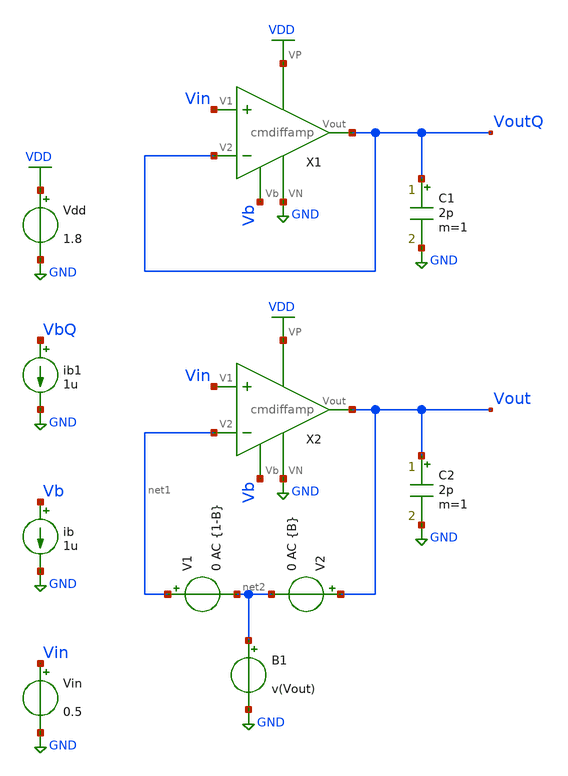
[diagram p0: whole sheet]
** sch_path: projects/current_mirror_diff_amp/xschem_ngspice/cmdiffamp_loopgain.sch
**.subckt cmdiffamp_loopgain
X1 Vin VoutQ VoutQ VDD GND Vb cmdiffamp
Vin Vin GND 0.5
Vdd VDD GND 1.8
ib Vb GND 1u
C1 VoutQ GND 2p m=1
ib1 VbQ GND 1u
X2 Vin net1 Vout VDD GND Vb cmdiffamp
C2 Vout GND 2p m=1
V1 net1 net2 0 AC {1-B}
V2 Vout net2 0 AC {B}
B1 net2 GND v(Vout)
**** begin user architecture code



.lib /foss/pdks/sky130A/libs.tech/ngspice/sky130.lib.spice tt

.param B=0
.control
ac dec 20 1 1e12
alterparam B=1
reset
ac dec 20 1 1e12
setplot new
set curplottitle=Loopgain
let frequency=ac1.frequency
let T = (ac1.i(V2) + ac2.i(V1)) / (ac1.i(V1) + ac2.i(V2))
let Tmag = db(T)
let Tphase = 180*cph(T)/pi
plot Tmag Tphase xlog
.endc



**** end user architecture code
**.ends

* expanding   symbol:
*+  /foss/designs/my_design/projects/current_mirror_diff_amp/xschem_ngspice/cmdiffamp.sym # of pins=6
** sym_path: projects/current_mirror_diff_amp/xschem_ngspice/cmdiffamp.sym
** sch_path: projects/current_mirror_diff_amp/xschem_ngspice/cmdiffamp.sch
.subckt cmdiffamp V1 V2 Vout VP VN Vb
*.ipin V1
*.ipin V2
*.opin Vout
*.iopin VN
*.iopin Vb
*.iopin VP
XM1a net3 V1 net1 VDD sky130_fd_pr__pfet_01v8 L=0.5 W=3 nf=1 ad='int((nf+1)/2) * W/nf * 0.29' as='int((nf+2)/2) * W/nf * 0.29'
+ pd='2*int((nf+1)/2) * (W/nf + 0.29)' ps='2*int((nf+2)/2) * (W/nf + 0.29)' nrd='0.29 / W' nrs='0.29 / W'
+ sa=0 sb=0 sd=0 mult=1 m=1
XM2a net2 V2 net1 VDD sky130_fd_pr__pfet_01v8 L=0.5 W=3 nf=1 ad='int((nf+1)/2) * W/nf * 0.29' as='int((nf+2)/2) * W/nf * 0.29'
+ pd='2*int((nf+1)/2) * (W/nf + 0.29)' ps='2*int((nf+2)/2) * (W/nf + 0.29)' nrd='0.29 / W' nrs='0.29 / W'
+ sa=0 sb=0 sd=0 mult=1 m=1
XM2b net1 V2 net2 VDD sky130_fd_pr__pfet_01v8 L=0.5 W=3 nf=1 ad='int((nf+1)/2) * W/nf * 0.29' as='int((nf+2)/2) * W/nf * 0.29'
+ pd='2*int((nf+1)/2) * (W/nf + 0.29)' ps='2*int((nf+2)/2) * (W/nf + 0.29)' nrd='0.29 / W' nrs='0.29 / W'
+ sa=0 sb=0 sd=0 mult=1 m=1
XM1b net1 V1 net3 VDD sky130_fd_pr__pfet_01v8 L=0.5 W=3 nf=1 ad='int((nf+1)/2) * W/nf * 0.29' as='int((nf+2)/2) * W/nf * 0.29'
+ pd='2*int((nf+1)/2) * (W/nf + 0.29)' ps='2*int((nf+2)/2) * (W/nf + 0.29)' nrd='0.29 / W' nrs='0.29 / W'
+ sa=0 sb=0 sd=0 mult=1 m=1
XM1c net3 V1 net1 VDD sky130_fd_pr__pfet_01v8 L=0.5 W=3 nf=1 ad='int((nf+1)/2) * W/nf * 0.29' as='int((nf+2)/2) * W/nf * 0.29'
+ pd='2*int((nf+1)/2) * (W/nf + 0.29)' ps='2*int((nf+2)/2) * (W/nf + 0.29)' nrd='0.29 / W' nrs='0.29 / W'
+ sa=0 sb=0 sd=0 mult=1 m=1
XM2c net2 V2 net1 VDD sky130_fd_pr__pfet_01v8 L=0.5 W=3 nf=1 ad='int((nf+1)/2) * W/nf * 0.29' as='int((nf+2)/2) * W/nf * 0.29'
+ pd='2*int((nf+1)/2) * (W/nf + 0.29)' ps='2*int((nf+2)/2) * (W/nf + 0.29)' nrd='0.29 / W' nrs='0.29 / W'
+ sa=0 sb=0 sd=0 mult=1 m=1
XM2d net1 V2 net2 VDD sky130_fd_pr__pfet_01v8 L=0.5 W=3 nf=1 ad='int((nf+1)/2) * W/nf * 0.29' as='int((nf+2)/2) * W/nf * 0.29'
+ pd='2*int((nf+1)/2) * (W/nf + 0.29)' ps='2*int((nf+2)/2) * (W/nf + 0.29)' nrd='0.29 / W' nrs='0.29 / W'
+ sa=0 sb=0 sd=0 mult=1 m=1
XM1d net1 V1 net3 VDD sky130_fd_pr__pfet_01v8 L=0.5 W=3 nf=1 ad='int((nf+1)/2) * W/nf * 0.29' as='int((nf+2)/2) * W/nf * 0.29'
+ pd='2*int((nf+1)/2) * (W/nf + 0.29)' ps='2*int((nf+2)/2) * (W/nf + 0.29)' nrd='0.29 / W' nrs='0.29 / W'
+ sa=0 sb=0 sd=0 mult=1 m=1
XM5a net2 net2 VN GND sky130_fd_pr__nfet_01v8 L=0.5 W=3 nf=1 ad='int((nf+1)/2) * W/nf * 0.29' as='int((nf+2)/2) * W/nf * 0.29'
+ pd='2*int((nf+1)/2) * (W/nf + 0.29)' ps='2*int((nf+2)/2) * (W/nf + 0.29)' nrd='0.29 / W' nrs='0.29 / W'
+ sa=0 sb=0 sd=0 mult=1 m=1
XM6a VN net2 net4 GND sky130_fd_pr__nfet_01v8 L=0.5 W=3 nf=1 ad='int((nf+1)/2) * W/nf * 0.29' as='int((nf+2)/2) * W/nf * 0.29'
+ pd='2*int((nf+1)/2) * (W/nf + 0.29)' ps='2*int((nf+2)/2) * (W/nf + 0.29)' nrd='0.29 / W' nrs='0.29 / W'
+ sa=0 sb=0 sd=0 mult=1 m=1
XM6b net4 net2 VN GND sky130_fd_pr__nfet_01v8 L=0.5 W=3 nf=1 ad='int((nf+1)/2) * W/nf * 0.29' as='int((nf+2)/2) * W/nf * 0.29'
+ pd='2*int((nf+1)/2) * (W/nf + 0.29)' ps='2*int((nf+2)/2) * (W/nf + 0.29)' nrd='0.29 / W' nrs='0.29 / W'
+ sa=0 sb=0 sd=0 mult=1 m=1
XM5b VN net2 net2 GND sky130_fd_pr__nfet_01v8 L=0.5 W=3 nf=1 ad='int((nf+1)/2) * W/nf * 0.29' as='int((nf+2)/2) * W/nf * 0.29'
+ pd='2*int((nf+1)/2) * (W/nf + 0.29)' ps='2*int((nf+2)/2) * (W/nf + 0.29)' nrd='0.29 / W' nrs='0.29 / W'
+ sa=0 sb=0 sd=0 mult=1 m=1
XM5c net2 net2 VN GND sky130_fd_pr__nfet_01v8 L=0.5 W=3 nf=1 ad='int((nf+1)/2) * W/nf * 0.29' as='int((nf+2)/2) * W/nf * 0.29'
+ pd='2*int((nf+1)/2) * (W/nf + 0.29)' ps='2*int((nf+2)/2) * (W/nf + 0.29)' nrd='0.29 / W' nrs='0.29 / W'
+ sa=0 sb=0 sd=0 mult=1 m=1
XM6c VN net2 net4 GND sky130_fd_pr__nfet_01v8 L=0.5 W=3 nf=1 ad='int((nf+1)/2) * W/nf * 0.29' as='int((nf+2)/2) * W/nf * 0.29'
+ pd='2*int((nf+1)/2) * (W/nf + 0.29)' ps='2*int((nf+2)/2) * (W/nf + 0.29)' nrd='0.29 / W' nrs='0.29 / W'
+ sa=0 sb=0 sd=0 mult=1 m=1
XM6d net4 net2 VN GND sky130_fd_pr__nfet_01v8 L=0.5 W=3 nf=1 ad='int((nf+1)/2) * W/nf * 0.29' as='int((nf+2)/2) * W/nf * 0.29'
+ pd='2*int((nf+1)/2) * (W/nf + 0.29)' ps='2*int((nf+2)/2) * (W/nf + 0.29)' nrd='0.29 / W' nrs='0.29 / W'
+ sa=0 sb=0 sd=0 mult=1 m=1
XM5d VN net2 net2 GND sky130_fd_pr__nfet_01v8 L=0.5 W=3 nf=1 ad='int((nf+1)/2) * W/nf * 0.29' as='int((nf+2)/2) * W/nf * 0.29'
+ pd='2*int((nf+1)/2) * (W/nf + 0.29)' ps='2*int((nf+2)/2) * (W/nf + 0.29)' nrd='0.29 / W' nrs='0.29 / W'
+ sa=0 sb=0 sd=0 mult=1 m=1
XM3a net3 net3 VN GND sky130_fd_pr__nfet_01v8 L=0.5 W=3 nf=1 ad='int((nf+1)/2) * W/nf * 0.29' as='int((nf+2)/2) * W/nf * 0.29'
+ pd='2*int((nf+1)/2) * (W/nf + 0.29)' ps='2*int((nf+2)/2) * (W/nf + 0.29)' nrd='0.29 / W' nrs='0.29 / W'
+ sa=0 sb=0 sd=0 mult=1 m=1
XM4a VN net3 Vout GND sky130_fd_pr__nfet_01v8 L=0.5 W=3 nf=1 ad='int((nf+1)/2) * W/nf * 0.29' as='int((nf+2)/2) * W/nf * 0.29'
+ pd='2*int((nf+1)/2) * (W/nf + 0.29)' ps='2*int((nf+2)/2) * (W/nf + 0.29)' nrd='0.29 / W' nrs='0.29 / W'
+ sa=0 sb=0 sd=0 mult=1 m=1
XM4b Vout net3 VN GND sky130_fd_pr__nfet_01v8 L=0.5 W=3 nf=1 ad='int((nf+1)/2) * W/nf * 0.29' as='int((nf+2)/2) * W/nf * 0.29'
+ pd='2*int((nf+1)/2) * (W/nf + 0.29)' ps='2*int((nf+2)/2) * (W/nf + 0.29)' nrd='0.29 / W' nrs='0.29 / W'
+ sa=0 sb=0 sd=0 mult=1 m=1
XM3b VN net3 net3 GND sky130_fd_pr__nfet_01v8 L=0.5 W=3 nf=1 ad='int((nf+1)/2) * W/nf * 0.29' as='int((nf+2)/2) * W/nf * 0.29'
+ pd='2*int((nf+1)/2) * (W/nf + 0.29)' ps='2*int((nf+2)/2) * (W/nf + 0.29)' nrd='0.29 / W' nrs='0.29 / W'
+ sa=0 sb=0 sd=0 mult=1 m=1
XM3c net3 net3 VN GND sky130_fd_pr__nfet_01v8 L=0.5 W=3 nf=1 ad='int((nf+1)/2) * W/nf * 0.29' as='int((nf+2)/2) * W/nf * 0.29'
+ pd='2*int((nf+1)/2) * (W/nf + 0.29)' ps='2*int((nf+2)/2) * (W/nf + 0.29)' nrd='0.29 / W' nrs='0.29 / W'
+ sa=0 sb=0 sd=0 mult=1 m=1
XM4c VN net3 Vout GND sky130_fd_pr__nfet_01v8 L=0.5 W=3 nf=1 ad='int((nf+1)/2) * W/nf * 0.29' as='int((nf+2)/2) * W/nf * 0.29'
+ pd='2*int((nf+1)/2) * (W/nf + 0.29)' ps='2*int((nf+2)/2) * (W/nf + 0.29)' nrd='0.29 / W' nrs='0.29 / W'
+ sa=0 sb=0 sd=0 mult=1 m=1
XM4d Vout net3 VN GND sky130_fd_pr__nfet_01v8 L=0.5 W=3 nf=1 ad='int((nf+1)/2) * W/nf * 0.29' as='int((nf+2)/2) * W/nf * 0.29'
+ pd='2*int((nf+1)/2) * (W/nf + 0.29)' ps='2*int((nf+2)/2) * (W/nf + 0.29)' nrd='0.29 / W' nrs='0.29 / W'
+ sa=0 sb=0 sd=0 mult=1 m=1
XM3d VN net3 net3 GND sky130_fd_pr__nfet_01v8 L=0.5 W=3 nf=1 ad='int((nf+1)/2) * W/nf * 0.29' as='int((nf+2)/2) * W/nf * 0.29'
+ pd='2*int((nf+1)/2) * (W/nf + 0.29)' ps='2*int((nf+2)/2) * (W/nf + 0.29)' nrd='0.29 / W' nrs='0.29 / W'
+ sa=0 sb=0 sd=0 mult=1 m=1
XM7a net4 net4 VP VDD sky130_fd_pr__pfet_01v8 L=0.5 W=3 nf=1 ad='int((nf+1)/2) * W/nf * 0.29' as='int((nf+2)/2) * W/nf * 0.29'
+ pd='2*int((nf+1)/2) * (W/nf + 0.29)' ps='2*int((nf+2)/2) * (W/nf + 0.29)' nrd='0.29 / W' nrs='0.29 / W'
+ sa=0 sb=0 sd=0 mult=1 m=1
XM8a VP net4 Vout VDD sky130_fd_pr__pfet_01v8 L=0.5 W=3 nf=1 ad='int((nf+1)/2) * W/nf * 0.29' as='int((nf+2)/2) * W/nf * 0.29'
+ pd='2*int((nf+1)/2) * (W/nf + 0.29)' ps='2*int((nf+2)/2) * (W/nf + 0.29)' nrd='0.29 / W' nrs='0.29 / W'
+ sa=0 sb=0 sd=0 mult=1 m=1
XM8b Vout net4 VP VDD sky130_fd_pr__pfet_01v8 L=0.5 W=3 nf=1 ad='int((nf+1)/2) * W/nf * 0.29' as='int((nf+2)/2) * W/nf * 0.29'
+ pd='2*int((nf+1)/2) * (W/nf + 0.29)' ps='2*int((nf+2)/2) * (W/nf + 0.29)' nrd='0.29 / W' nrs='0.29 / W'
+ sa=0 sb=0 sd=0 mult=1 m=1
XM7b VP net4 net4 VDD sky130_fd_pr__pfet_01v8 L=0.5 W=3 nf=1 ad='int((nf+1)/2) * W/nf * 0.29' as='int((nf+2)/2) * W/nf * 0.29'
+ pd='2*int((nf+1)/2) * (W/nf + 0.29)' ps='2*int((nf+2)/2) * (W/nf + 0.29)' nrd='0.29 / W' nrs='0.29 / W'
+ sa=0 sb=0 sd=0 mult=1 m=1
XM7c net4 net4 VP VDD sky130_fd_pr__pfet_01v8 L=0.5 W=3 nf=1 ad='int((nf+1)/2) * W/nf * 0.29' as='int((nf+2)/2) * W/nf * 0.29'
+ pd='2*int((nf+1)/2) * (W/nf + 0.29)' ps='2*int((nf+2)/2) * (W/nf + 0.29)' nrd='0.29 / W' nrs='0.29 / W'
+ sa=0 sb=0 sd=0 mult=1 m=1
XM8c VP net4 Vout VDD sky130_fd_pr__pfet_01v8 L=0.5 W=3 nf=1 ad='int((nf+1)/2) * W/nf * 0.29' as='int((nf+2)/2) * W/nf * 0.29'
+ pd='2*int((nf+1)/2) * (W/nf + 0.29)' ps='2*int((nf+2)/2) * (W/nf + 0.29)' nrd='0.29 / W' nrs='0.29 / W'
+ sa=0 sb=0 sd=0 mult=1 m=1
XM8d Vout net4 VP VDD sky130_fd_pr__pfet_01v8 L=0.5 W=3 nf=1 ad='int((nf+1)/2) * W/nf * 0.29' as='int((nf+2)/2) * W/nf * 0.29'
+ pd='2*int((nf+1)/2) * (W/nf + 0.29)' ps='2*int((nf+2)/2) * (W/nf + 0.29)' nrd='0.29 / W' nrs='0.29 / W'
+ sa=0 sb=0 sd=0 mult=1 m=1
XM7d VP net4 net4 VDD sky130_fd_pr__pfet_01v8 L=0.5 W=3 nf=1 ad='int((nf+1)/2) * W/nf * 0.29' as='int((nf+2)/2) * W/nf * 0.29'
+ pd='2*int((nf+1)/2) * (W/nf + 0.29)' ps='2*int((nf+2)/2) * (W/nf + 0.29)' nrd='0.29 / W' nrs='0.29 / W'
+ sa=0 sb=0 sd=0 mult=1 m=1
XM9a Vb Vb VP VDD sky130_fd_pr__pfet_01v8 L=0.5 W=1.5 nf=1 ad='int((nf+1)/2) * W/nf * 0.29' as='int((nf+2)/2) * W/nf * 0.29'
+ pd='2*int((nf+1)/2) * (W/nf + 0.29)' ps='2*int((nf+2)/2) * (W/nf + 0.29)' nrd='0.29 / W' nrs='0.29 / W'
+ sa=0 sb=0 sd=0 mult=1 m=1
XM10a VP Vb net1 VDD sky130_fd_pr__pfet_01v8 L=0.5 W=1.5 nf=1 ad='int((nf+1)/2) * W/nf * 0.29' as='int((nf+2)/2) * W/nf * 0.29'
+ pd='2*int((nf+1)/2) * (W/nf + 0.29)' ps='2*int((nf+2)/2) * (W/nf + 0.29)' nrd='0.29 / W' nrs='0.29 / W'
+ sa=0 sb=0 sd=0 mult=1 m=1
XM10b net1 Vb VP VDD sky130_fd_pr__pfet_01v8 L=0.5 W=1.5 nf=1 ad='int((nf+1)/2) * W/nf * 0.29' as='int((nf+2)/2) * W/nf * 0.29'
+ pd='2*int((nf+1)/2) * (W/nf + 0.29)' ps='2*int((nf+2)/2) * (W/nf + 0.29)' nrd='0.29 / W' nrs='0.29 / W'
+ sa=0 sb=0 sd=0 mult=1 m=1
XM9b VP Vb Vb VDD sky130_fd_pr__pfet_01v8 L=0.5 W=1.5 nf=1 ad='int((nf+1)/2) * W/nf * 0.29' as='int((nf+2)/2) * W/nf * 0.29'
+ pd='2*int((nf+1)/2) * (W/nf + 0.29)' ps='2*int((nf+2)/2) * (W/nf + 0.29)' nrd='0.29 / W' nrs='0.29 / W'
+ sa=0 sb=0 sd=0 mult=1 m=1
XM9c Vb Vb VP VDD sky130_fd_pr__pfet_01v8 L=0.5 W=1.5 nf=1 ad='int((nf+1)/2) * W/nf * 0.29' as='int((nf+2)/2) * W/nf * 0.29'
+ pd='2*int((nf+1)/2) * (W/nf + 0.29)' ps='2*int((nf+2)/2) * (W/nf + 0.29)' nrd='0.29 / W' nrs='0.29 / W'
+ sa=0 sb=0 sd=0 mult=1 m=1
XM10c VP Vb net1 VDD sky130_fd_pr__pfet_01v8 L=0.5 W=1.5 nf=1 ad='int((nf+1)/2) * W/nf * 0.29' as='int((nf+2)/2) * W/nf * 0.29'
+ pd='2*int((nf+1)/2) * (W/nf + 0.29)' ps='2*int((nf+2)/2) * (W/nf + 0.29)' nrd='0.29 / W' nrs='0.29 / W'
+ sa=0 sb=0 sd=0 mult=1 m=1
XM10d net1 Vb VP VDD sky130_fd_pr__pfet_01v8 L=0.5 W=1.5 nf=1 ad='int((nf+1)/2) * W/nf * 0.29' as='int((nf+2)/2) * W/nf * 0.29'
+ pd='2*int((nf+1)/2) * (W/nf + 0.29)' ps='2*int((nf+2)/2) * (W/nf + 0.29)' nrd='0.29 / W' nrs='0.29 / W'
+ sa=0 sb=0 sd=0 mult=1 m=1
XM9d VP Vb Vb VDD sky130_fd_pr__pfet_01v8 L=0.5 W=1.5 nf=1 ad='int((nf+1)/2) * W/nf * 0.29' as='int((nf+2)/2) * W/nf * 0.29'
+ pd='2*int((nf+1)/2) * (W/nf + 0.29)' ps='2*int((nf+2)/2) * (W/nf + 0.29)' nrd='0.29 / W' nrs='0.29 / W'
+ sa=0 sb=0 sd=0 mult=1 m=1
XM9e Vb Vb VP VDD sky130_fd_pr__pfet_01v8 L=0.5 W=1.5 nf=1 ad='int((nf+1)/2) * W/nf * 0.29' as='int((nf+2)/2) * W/nf * 0.29'
+ pd='2*int((nf+1)/2) * (W/nf + 0.29)' ps='2*int((nf+2)/2) * (W/nf + 0.29)' nrd='0.29 / W' nrs='0.29 / W'
+ sa=0 sb=0 sd=0 mult=1 m=1
XM10e VP Vb net1 VDD sky130_fd_pr__pfet_01v8 L=0.5 W=1.5 nf=1 ad='int((nf+1)/2) * W/nf * 0.29' as='int((nf+2)/2) * W/nf * 0.29'
+ pd='2*int((nf+1)/2) * (W/nf + 0.29)' ps='2*int((nf+2)/2) * (W/nf + 0.29)' nrd='0.29 / W' nrs='0.29 / W'
+ sa=0 sb=0 sd=0 mult=1 m=1
XM10f net1 Vb VP VDD sky130_fd_pr__pfet_01v8 L=0.5 W=1.5 nf=1 ad='int((nf+1)/2) * W/nf * 0.29' as='int((nf+2)/2) * W/nf * 0.29'
+ pd='2*int((nf+1)/2) * (W/nf + 0.29)' ps='2*int((nf+2)/2) * (W/nf + 0.29)' nrd='0.29 / W' nrs='0.29 / W'
+ sa=0 sb=0 sd=0 mult=1 m=1
XM9f VP Vb Vb VDD sky130_fd_pr__pfet_01v8 L=0.5 W=1.5 nf=1 ad='int((nf+1)/2) * W/nf * 0.29' as='int((nf+2)/2) * W/nf * 0.29'
+ pd='2*int((nf+1)/2) * (W/nf + 0.29)' ps='2*int((nf+2)/2) * (W/nf + 0.29)' nrd='0.29 / W' nrs='0.29 / W'
+ sa=0 sb=0 sd=0 mult=1 m=1
XM9g Vb Vb VP VDD sky130_fd_pr__pfet_01v8 L=0.5 W=1.5 nf=1 ad='int((nf+1)/2) * W/nf * 0.29' as='int((nf+2)/2) * W/nf * 0.29'
+ pd='2*int((nf+1)/2) * (W/nf + 0.29)' ps='2*int((nf+2)/2) * (W/nf + 0.29)' nrd='0.29 / W' nrs='0.29 / W'
+ sa=0 sb=0 sd=0 mult=1 m=1
XM10g VP Vb net1 VDD sky130_fd_pr__pfet_01v8 L=0.5 W=1.5 nf=1 ad='int((nf+1)/2) * W/nf * 0.29' as='int((nf+2)/2) * W/nf * 0.29'
+ pd='2*int((nf+1)/2) * (W/nf + 0.29)' ps='2*int((nf+2)/2) * (W/nf + 0.29)' nrd='0.29 / W' nrs='0.29 / W'
+ sa=0 sb=0 sd=0 mult=1 m=1
XM10h net1 Vb VP VDD sky130_fd_pr__pfet_01v8 L=0.5 W=1.5 nf=1 ad='int((nf+1)/2) * W/nf * 0.29' as='int((nf+2)/2) * W/nf * 0.29'
+ pd='2*int((nf+1)/2) * (W/nf + 0.29)' ps='2*int((nf+2)/2) * (W/nf + 0.29)' nrd='0.29 / W' nrs='0.29 / W'
+ sa=0 sb=0 sd=0 mult=1 m=1
XM9h VP Vb Vb VDD sky130_fd_pr__pfet_01v8 L=0.5 W=1.5 nf=1 ad='int((nf+1)/2) * W/nf * 0.29' as='int((nf+2)/2) * W/nf * 0.29'
+ pd='2*int((nf+1)/2) * (W/nf + 0.29)' ps='2*int((nf+2)/2) * (W/nf + 0.29)' nrd='0.29 / W' nrs='0.29 / W'
+ sa=0 sb=0 sd=0 mult=1 m=1
XM1 VP VP Vb VDD sky130_fd_pr__pfet_01v8 L=0.5 W=1.5 nf=1 ad='int((nf+1)/2) * W/nf * 0.29' as='int((nf+2)/2) * W/nf * 0.29'
+ pd='2*int((nf+1)/2) * (W/nf + 0.29)' ps='2*int((nf+2)/2) * (W/nf + 0.29)' nrd='0.29 / W' nrs='0.29 / W'
+ sa=0 sb=0 sd=0 mult=1 m=1
XM2 Vb VP VP VDD sky130_fd_pr__pfet_01v8 L=0.5 W=1.5 nf=1 ad='int((nf+1)/2) * W/nf * 0.29' as='int((nf+2)/2) * W/nf * 0.29'
+ pd='2*int((nf+1)/2) * (W/nf + 0.29)' ps='2*int((nf+2)/2) * (W/nf + 0.29)' nrd='0.29 / W' nrs='0.29 / W'
+ sa=0 sb=0 sd=0 mult=1 m=1
XM3 VP VP Vb VDD sky130_fd_pr__pfet_01v8 L=0.5 W=1.5 nf=1 ad='int((nf+1)/2) * W/nf * 0.29' as='int((nf+2)/2) * W/nf * 0.29'
+ pd='2*int((nf+1)/2) * (W/nf + 0.29)' ps='2*int((nf+2)/2) * (W/nf + 0.29)' nrd='0.29 / W' nrs='0.29 / W'
+ sa=0 sb=0 sd=0 mult=1 m=1
XM4 Vb VP VP VDD sky130_fd_pr__pfet_01v8 L=0.5 W=1.5 nf=1 ad='int((nf+1)/2) * W/nf * 0.29' as='int((nf+2)/2) * W/nf * 0.29'
+ pd='2*int((nf+1)/2) * (W/nf + 0.29)' ps='2*int((nf+2)/2) * (W/nf + 0.29)' nrd='0.29 / W' nrs='0.29 / W'
+ sa=0 sb=0 sd=0 mult=1 m=1
XM5 net4 VP VP VDD sky130_fd_pr__pfet_01v8 L=0.5 W=3 nf=1 ad='int((nf+1)/2) * W/nf * 0.29' as='int((nf+2)/2) * W/nf * 0.29'
+ pd='2*int((nf+1)/2) * (W/nf + 0.29)' ps='2*int((nf+2)/2) * (W/nf + 0.29)' nrd='0.29 / W' nrs='0.29 / W'
+ sa=0 sb=0 sd=0 mult=1 m=1
XM6 net3 VP VP VDD sky130_fd_pr__pfet_01v8 L=0.5 W=3 nf=1 ad='int((nf+1)/2) * W/nf * 0.29' as='int((nf+2)/2) * W/nf * 0.29'
+ pd='2*int((nf+1)/2) * (W/nf + 0.29)' ps='2*int((nf+2)/2) * (W/nf + 0.29)' nrd='0.29 / W' nrs='0.29 / W'
+ sa=0 sb=0 sd=0 mult=1 m=1
XM7 VP VP net4 VDD sky130_fd_pr__pfet_01v8 L=0.5 W=3 nf=1 ad='int((nf+1)/2) * W/nf * 0.29' as='int((nf+2)/2) * W/nf * 0.29'
+ pd='2*int((nf+1)/2) * (W/nf + 0.29)' ps='2*int((nf+2)/2) * (W/nf + 0.29)' nrd='0.29 / W' nrs='0.29 / W'
+ sa=0 sb=0 sd=0 mult=1 m=1
XM8 net2 VN VN GND sky130_fd_pr__nfet_01v8 L=0.5 W=3 nf=1 ad='int((nf+1)/2) * W/nf * 0.29' as='int((nf+2)/2) * W/nf * 0.29'
+ pd='2*int((nf+1)/2) * (W/nf + 0.29)' ps='2*int((nf+2)/2) * (W/nf + 0.29)' nrd='0.29 / W' nrs='0.29 / W'
+ sa=0 sb=0 sd=0 mult=1 m=1
XM9 VN VN net3 GND sky130_fd_pr__nfet_01v8 L=0.5 W=3 nf=1 ad='int((nf+1)/2) * W/nf * 0.29' as='int((nf+2)/2) * W/nf * 0.29'
+ pd='2*int((nf+1)/2) * (W/nf + 0.29)' ps='2*int((nf+2)/2) * (W/nf + 0.29)' nrd='0.29 / W' nrs='0.29 / W'
+ sa=0 sb=0 sd=0 mult=1 m=1
XM10 net3 VP VP VDD sky130_fd_pr__pfet_01v8 L=0.5 W=3 nf=1 ad='int((nf+1)/2) * W/nf * 0.29' as='int((nf+2)/2) * W/nf * 0.29'
+ pd='2*int((nf+1)/2) * (W/nf + 0.29)' ps='2*int((nf+2)/2) * (W/nf + 0.29)' nrd='0.29 / W' nrs='0.29 / W'
+ sa=0 sb=0 sd=0 mult=1 m=1
XM11 VN VN net2 GND sky130_fd_pr__nfet_01v8 L=0.5 W=3 nf=1 ad='int((nf+1)/2) * W/nf * 0.29' as='int((nf+2)/2) * W/nf * 0.29'
+ pd='2*int((nf+1)/2) * (W/nf + 0.29)' ps='2*int((nf+2)/2) * (W/nf + 0.29)' nrd='0.29 / W' nrs='0.29 / W'
+ sa=0 sb=0 sd=0 mult=1 m=1
XM12 net3 VN VN GND sky130_fd_pr__nfet_01v8 L=0.5 W=3 nf=1 ad='int((nf+1)/2) * W/nf * 0.29' as='int((nf+2)/2) * W/nf * 0.29'
+ pd='2*int((nf+1)/2) * (W/nf + 0.29)' ps='2*int((nf+2)/2) * (W/nf + 0.29)' nrd='0.29 / W' nrs='0.29 / W'
+ sa=0 sb=0 sd=0 mult=1 m=1
.ends

.GLOBAL VDD
.GLOBAL GND
.end
